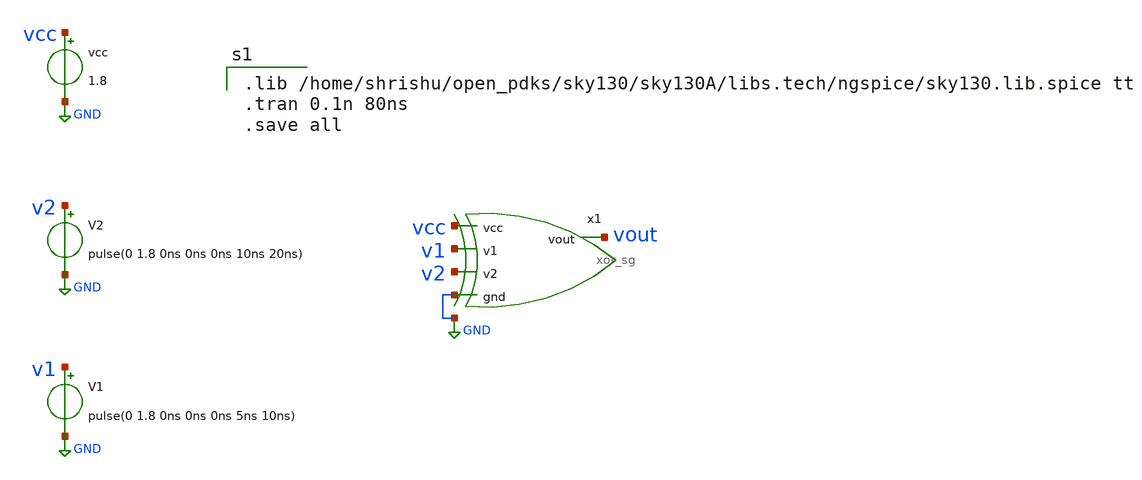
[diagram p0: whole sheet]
** sch_path: Logic_gates_using_cmos/xor_sg_test.sch
**.subckt xor_sg_test
x1 vcc v1 vout v2 GND xor_sg
vcc vcc GND 1.8
V1 v1 GND pulse(0 1.8 0ns 0ns 0ns 5ns 10ns)
V2 v2 GND pulse(0 1.8 0ns 0ns 0ns 10ns 20ns)
**** begin user architecture code

.lib /home/shrishu/open_pdks/sky130/sky130A/libs.tech/ngspice/sky130.lib.spice tt
.tran 0.1n 80ns
.save all

**** end user architecture code
**.ends

* expanding   symbol:  xor_sg.sym # of pins=5
** sym_path: Logic_gates_using_cmos/xor_sg.sym
** sch_path: Logic_gates_using_cmos/xor_sg.sch
.subckt xor_sg vcc v1 vout v2 gnd
*.ipin vcc
*.opin vout
*.ipin v1
*.ipin v2
*.ipin gnd
x2 vcc v1 net2 net1 gnd Nand_Cmos
x3 vcc net2 vout net3 gnd Nand_Cmos
x4 vcc net1 net3 v2 gnd Nand_Cmos
x1 vcc v1 net1 v2 gnd Nand_Cmos
.ends


* expanding   symbol:  xschem_circuits/Nand_Cmos.sym # of pins=5
** sym_path: Logic_gates_using_cmos/Nand_Cmos.sym
** sch_path: Logic_gates_using_cmos/Nand_Cmos.sch
.subckt Nand_Cmos VDD A out B gnd
*.ipin B
*.ipin A
*.ipin VDD
*.ipin gnd
*.opin out
XM2 net2 A VDD VDD sky130_fd_pr__pfet_01v8 L=0.15 W=4 nf=1 ad='int((nf+1)/2) * W/nf * 0.29' as='int((nf+2)/2) * W/nf * 0.29'
+ pd='2*int((nf+1)/2) * (W/nf + 0.29)' ps='2*int((nf+2)/2) * (W/nf + 0.29)' nrd='0.29 / W' nrs='0.29 / W'
+ sa=0 sb=0 sd=0 mult=1 m=1
XM1 net2 A net1 gnd sky130_fd_pr__nfet_01v8 L=0.15 W=2 nf=1 ad='int((nf+1)/2) * W/nf * 0.29' as='int((nf+2)/2) * W/nf * 0.29'
+ pd='2*int((nf+1)/2) * (W/nf + 0.29)' ps='2*int((nf+2)/2) * (W/nf + 0.29)' nrd='0.29 / W' nrs='0.29 / W'
+ sa=0 sb=0 sd=0 mult=1 m=1
XM3 net1 B gnd gnd sky130_fd_pr__nfet_01v8 L=0.15 W=2 nf=1 ad='int((nf+1)/2) * W/nf * 0.29' as='int((nf+2)/2) * W/nf * 0.29'
+ pd='2*int((nf+1)/2) * (W/nf + 0.29)' ps='2*int((nf+2)/2) * (W/nf + 0.29)' nrd='0.29 / W' nrs='0.29 / W'
+ sa=0 sb=0 sd=0 mult=1 m=1
XM4 net2 B VDD VDD sky130_fd_pr__pfet_01v8 L=0.15 W=4 nf=1 ad='int((nf+1)/2) * W/nf * 0.29' as='int((nf+2)/2) * W/nf * 0.29'
+ pd='2*int((nf+1)/2) * (W/nf + 0.29)' ps='2*int((nf+2)/2) * (W/nf + 0.29)' nrd='0.29 / W' nrs='0.29 / W'
+ sa=0 sb=0 sd=0 mult=1 m=1
C1 out gnd 0.12p m=1
R1 out net2 40 m=1
.ends

.GLOBAL GND
.end
